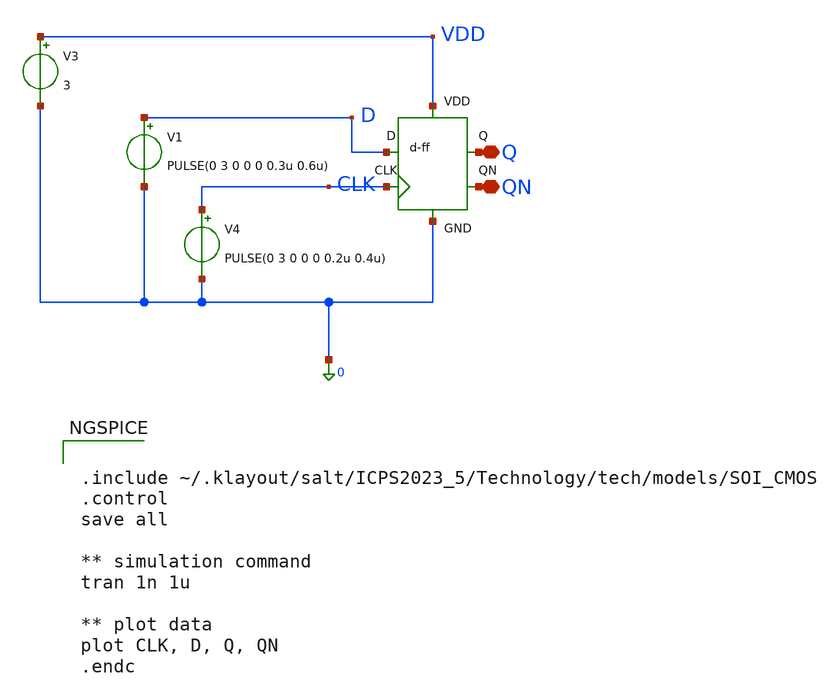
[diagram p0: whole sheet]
** sch_path: schematic/d-ff_tb.sch
**.subckt d-ff_tb Q QN
*.iopin Q
*.iopin QN
V1 D 0 PULSE(0 3 0 0 0 0.3u 0.6u)
V3 VDD 0 3
V4 CLK 0 PULSE(0 3 0 0 0 0.2u 0.4u)
x1 CLK D Q 0 VDD QN d-ff
**** begin user architecture code


.include ~/.klayout/salt/ICPS2023_5/Technology/tech/models/SOI_CMOS
.control
save all

** simulation command
tran 1n 1u

** plot data
plot CLK, D, Q, QN
.endc


**** end user architecture code
**.ends
.end
